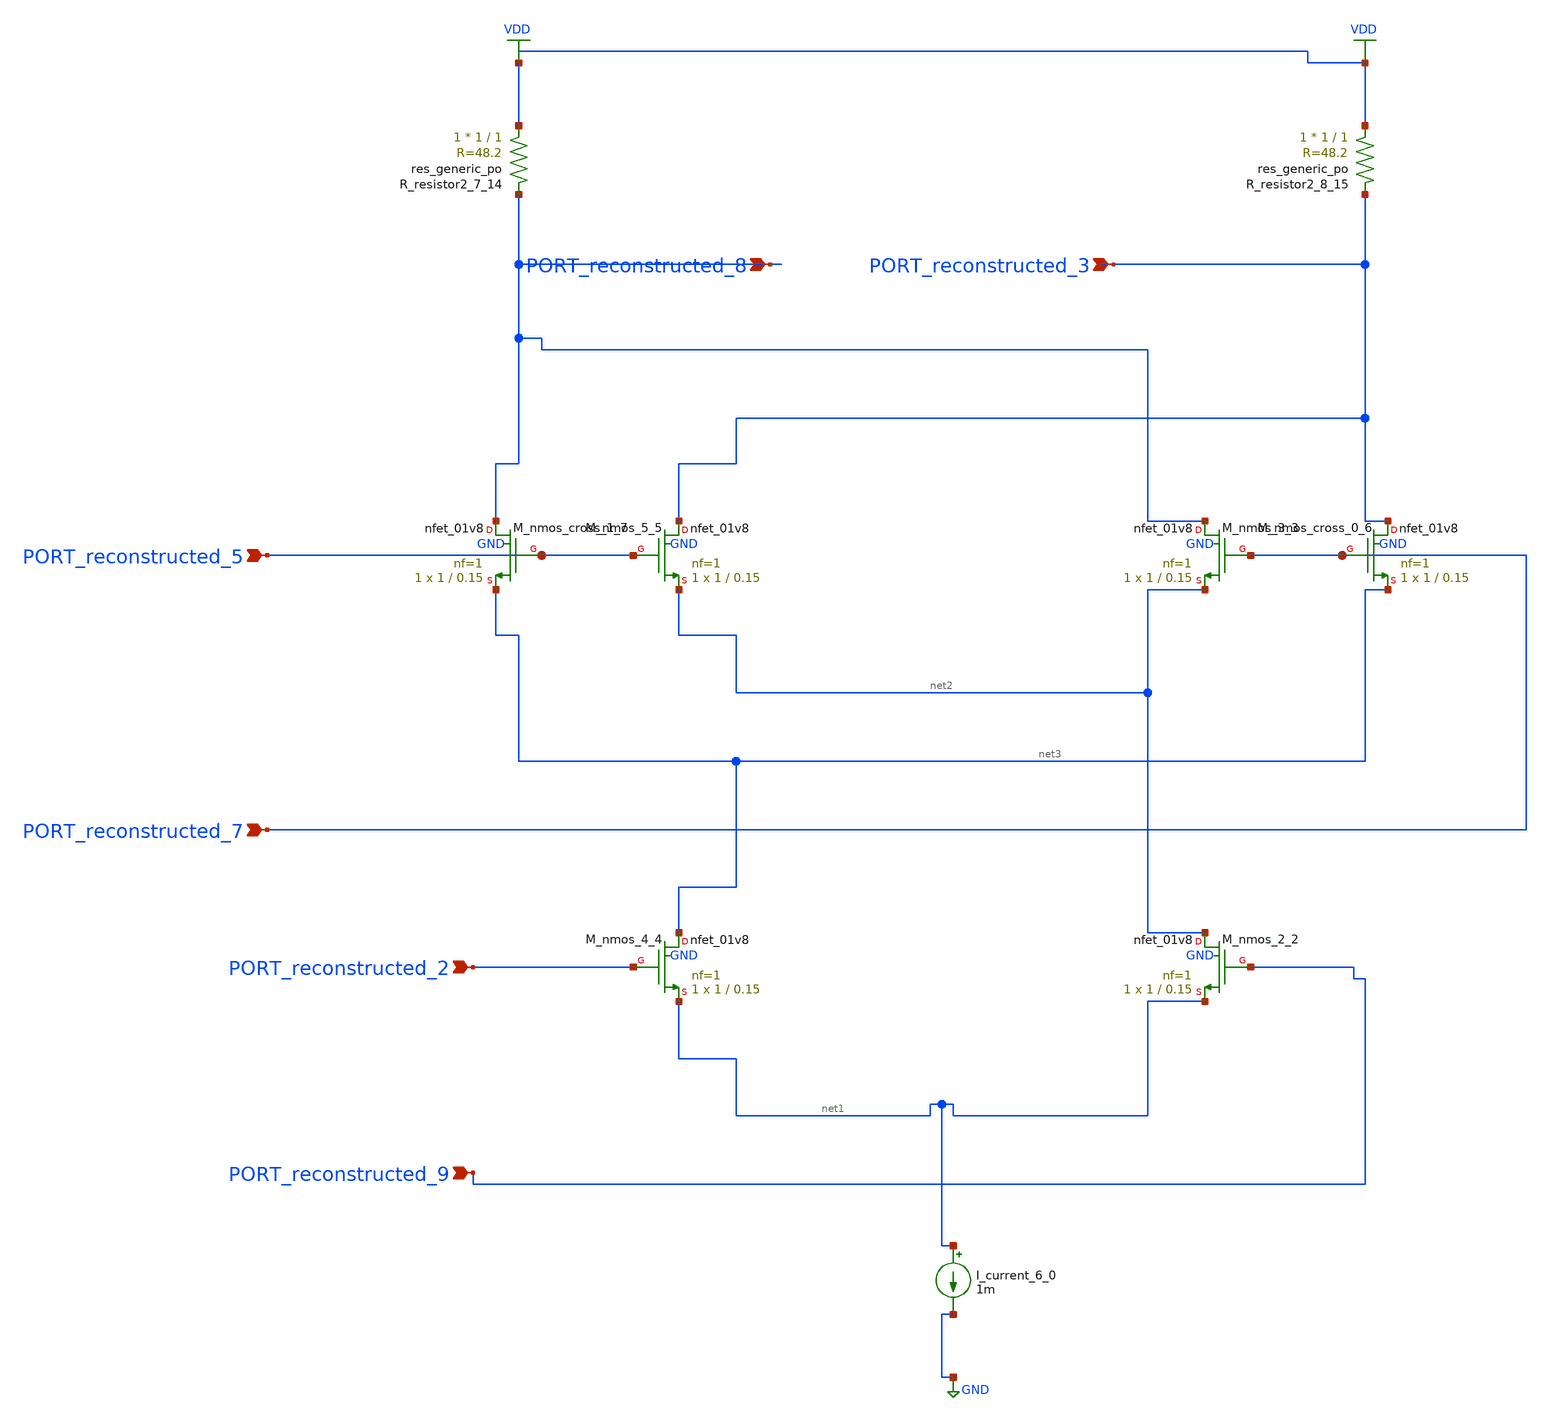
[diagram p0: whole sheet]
** sch_path: schematics/AMSNet/234.sch
**.subckt 234 PORT_reconstructed_8 PORT_reconstructed_3 PORT_reconstructed_5 PORT_reconstructed_2
*+ PORT_reconstructed_7 PORT_reconstructed_9
*.ipin PORT_reconstructed_8
*.ipin PORT_reconstructed_3
*.ipin PORT_reconstructed_5
*.ipin PORT_reconstructed_2
*.ipin PORT_reconstructed_7
*.ipin PORT_reconstructed_9
I_current_6_0 net1 GND 1m
XM_nmos_2_2 net2 PORT_reconstructed_9 net1 GND sky130_fd_pr__nfet_01v8 L=0.15 W=1 nf=1 ad='int((1 + 1)/2) * 1 / 1 * 0.29'
+ as='int((1 + 2)/2) * 1 / 1 * 0.29' pd='2*int((1 + 1)/2) * (1 / 1 + 0.29)' ps='2*int((1 + 2)/2) * (1 / 1 + 0.29)'
+ nrd='0.29 / 1 ' nrs='0.29 / 1 ' sa=0 sb=0 sd=0 mult=1 m=1
XM_nmos_3_3 PORT_reconstructed_8 PORT_reconstructed_7 net2 GND sky130_fd_pr__nfet_01v8 L=0.15 W=1 nf=1
+ ad='int((1 + 1)/2) * 1 / 1 * 0.29' as='int((1 + 2)/2) * 1 / 1 * 0.29' pd='2*int((1 + 1)/2) * (1 / 1 + 0.29)'
+ ps='2*int((1 + 2)/2) * (1 / 1 + 0.29)' nrd='0.29 / 1 ' nrs='0.29 / 1 ' sa=0 sb=0 sd=0 mult=1 m=1
XM_nmos_4_4 net3 PORT_reconstructed_2 net1 GND sky130_fd_pr__nfet_01v8 L=0.15 W=1 nf=1 ad='int((1 + 1)/2) * 1 / 1 * 0.29'
+ as='int((1 + 2)/2) * 1 / 1 * 0.29' pd='2*int((1 + 1)/2) * (1 / 1 + 0.29)' ps='2*int((1 + 2)/2) * (1 / 1 + 0.29)'
+ nrd='0.29 / 1 ' nrs='0.29 / 1 ' sa=0 sb=0 sd=0 mult=1 m=1
XM_nmos_5_5 PORT_reconstructed_3 PORT_reconstructed_5 net2 GND sky130_fd_pr__nfet_01v8 L=0.15 W=1 nf=1
+ ad='int((1 + 1)/2) * 1 / 1 * 0.29' as='int((1 + 2)/2) * 1 / 1 * 0.29' pd='2*int((1 + 1)/2) * (1 / 1 + 0.29)'
+ ps='2*int((1 + 2)/2) * (1 / 1 + 0.29)' nrd='0.29 / 1 ' nrs='0.29 / 1 ' sa=0 sb=0 sd=0 mult=1 m=1
XM_nmos_cross_0_6 PORT_reconstructed_3 PORT_reconstructed_7 net3 GND sky130_fd_pr__nfet_01v8 L=0.15 W=1
+ nf=1 ad='int((1 + 1)/2) * 1 / 1 * 0.29' as='int((1 + 2)/2) * 1 / 1 * 0.29' pd='2*int((1 + 1)/2) * (1 / 1 + 0.29)'
+ ps='2*int((1 + 2)/2) * (1 / 1 + 0.29)' nrd='0.29 / 1 ' nrs='0.29 / 1 ' sa=0 sb=0 sd=0 mult=1 m=1
XM_nmos_cross_1_7 PORT_reconstructed_8 PORT_reconstructed_5 net3 GND sky130_fd_pr__nfet_01v8 L=0.15 W=1
+ nf=1 ad='int((1 + 1)/2) * 1 / 1 * 0.29' as='int((1 + 2)/2) * 1 / 1 * 0.29' pd='2*int((1 + 1)/2) * (1 / 1 + 0.29)'
+ ps='2*int((1 + 2)/2) * (1 / 1 + 0.29)' nrd='0.29 / 1 ' nrs='0.29 / 1 ' sa=0 sb=0 sd=0 mult=1 m=1
XR_resistor2_7_14 VDD PORT_reconstructed_8 sky130_fd_pr__res_generic_po W=1 L=1 m=1
XR_resistor2_8_15 VDD PORT_reconstructed_3 sky130_fd_pr__res_generic_po W=1 L=1 m=1
**.ends
.GLOBAL GND
.GLOBAL VDD
.end
